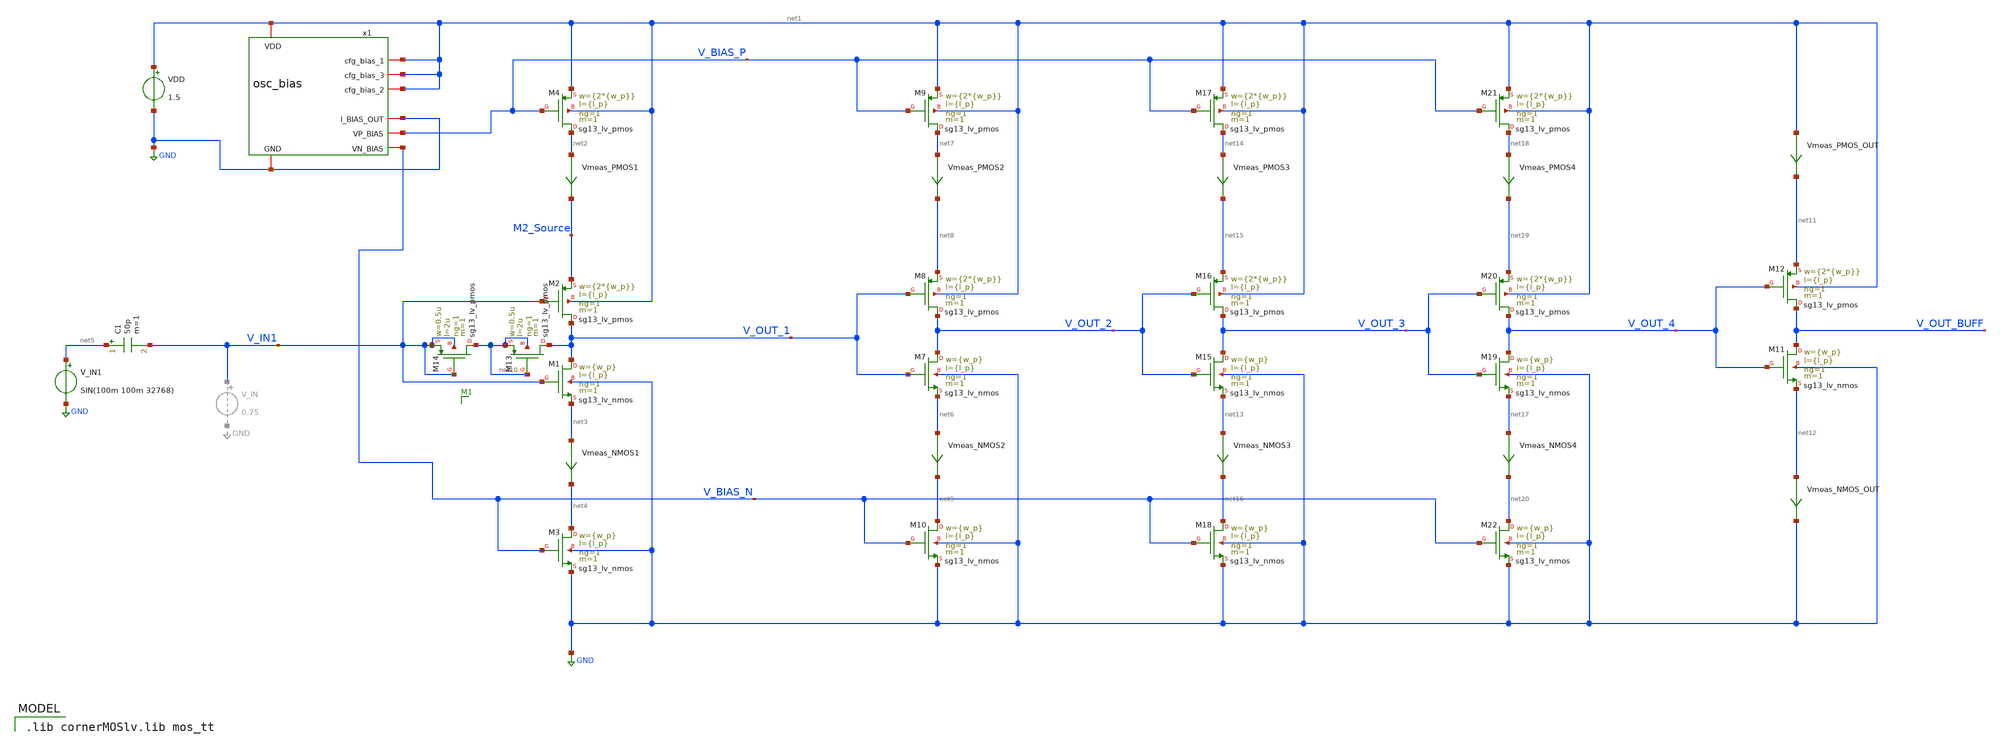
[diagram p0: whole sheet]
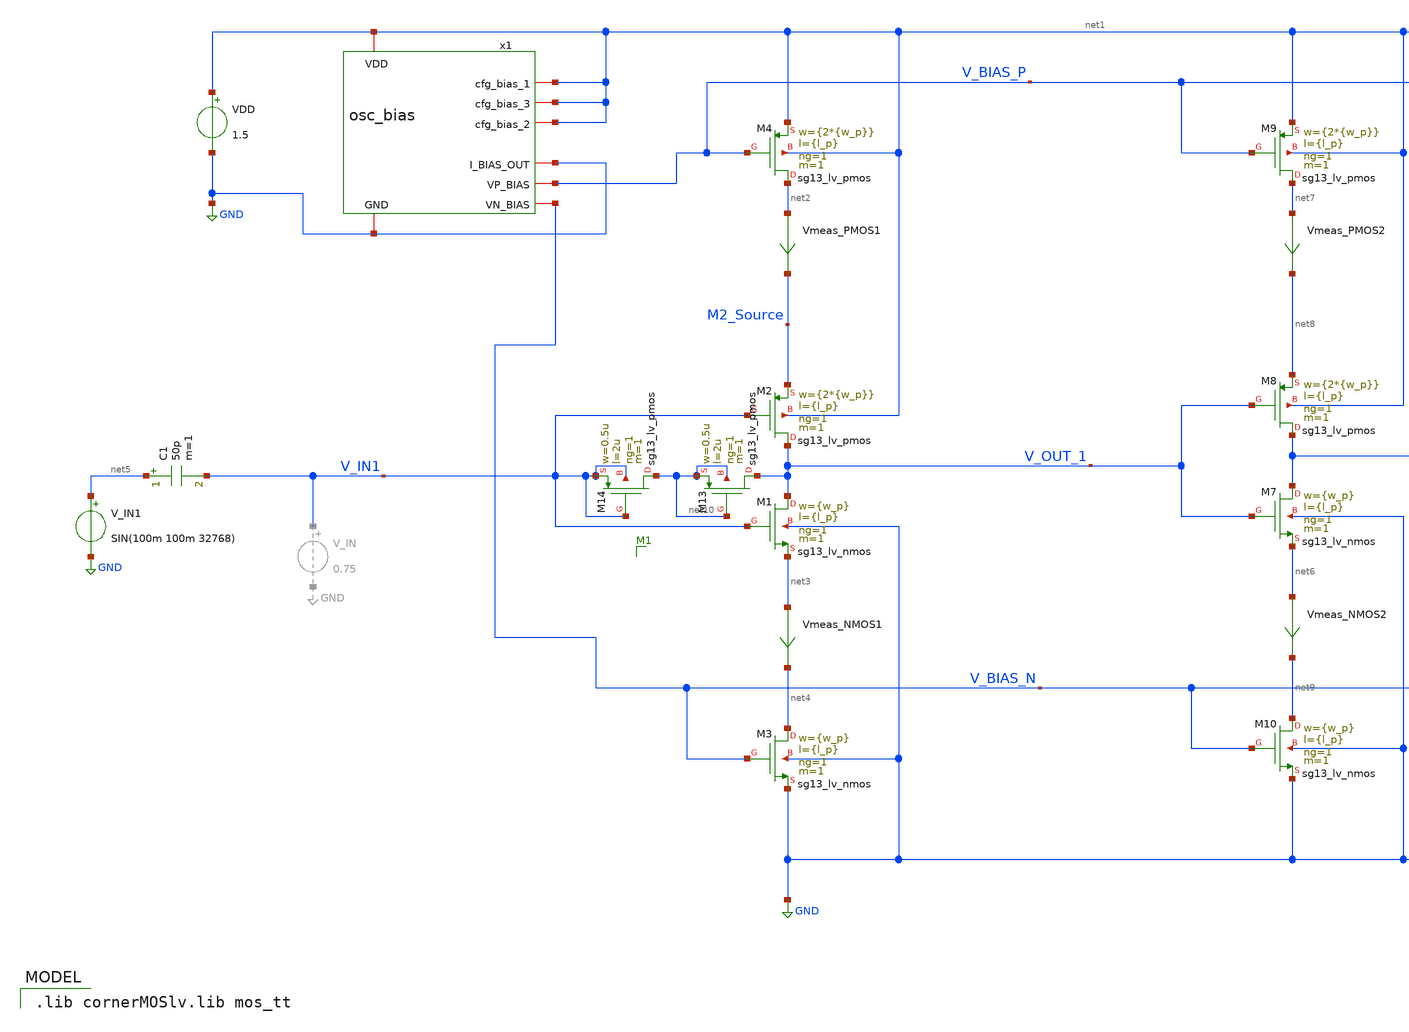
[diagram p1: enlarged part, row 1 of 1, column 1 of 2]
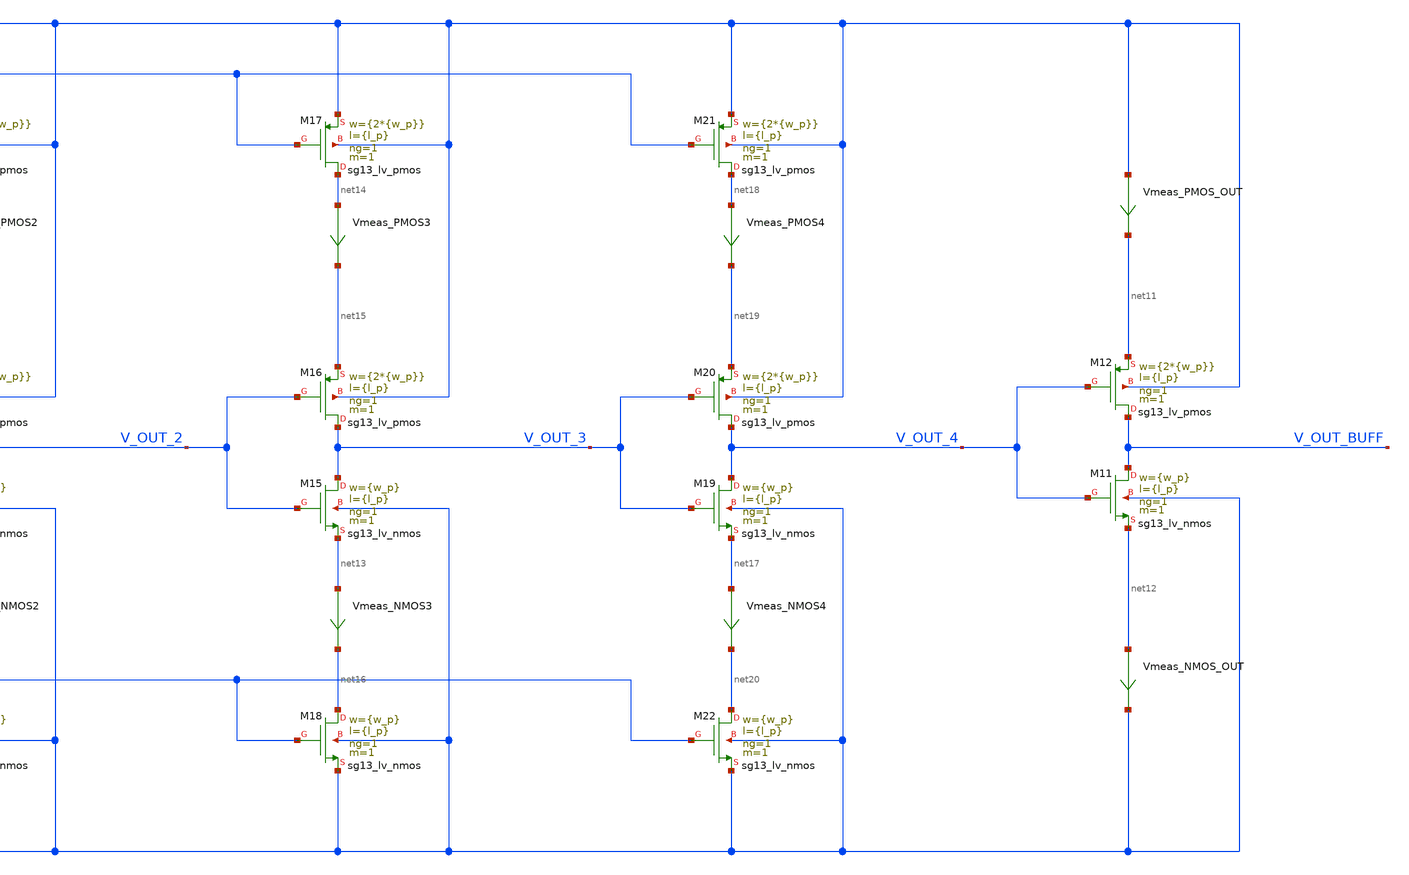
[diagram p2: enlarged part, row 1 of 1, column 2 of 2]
** sch_path: inverter_starved_v2_playground.sch
**.subckt inverter_starved_v2_playground
XM1 V_OUT_1 V_IN1 net3 GND sg13_lv_nmos w={w_p} l={l_p} ng=1 m=1 mm_ok=1
XM2 V_OUT_1 V_IN1 M2_Source net1 sg13_lv_pmos w={2*{w_p}} l={l_p} ng=1 m=1 mm_ok=1
VDD net1 GND 1.5
XM3 net4 V_BIAS_N GND GND sg13_lv_nmos w={w_p} l={l_p} ng=1 m=1 mm_ok=1
XM4 net2 V_BIAS_P net1 net1 sg13_lv_pmos w={2*{w_p}} l={l_p} ng=1 m=1 mm_ok=1
Vmeas_PMOS1 net2 M2_Source 0
.save i(vmeas_pmos1)
Vmeas_NMOS1 net3 net4 0
.save i(vmeas_nmos1)
V_IN1 net5 GND SIN(100m 100m 32768)
C1 net5 V_IN1 50p m=1
XM7 V_OUT_2 V_OUT_1 net6 GND sg13_lv_nmos w={w_p} l={l_p} ng=1 m=1 mm_ok=1
XM8 V_OUT_2 V_OUT_1 net8 net1 sg13_lv_pmos w={2*{w_p}} l={l_p} ng=1 m=1 mm_ok=1
Vmeas_NMOS2 net6 net9 0
.save i(vmeas_nmos2)
XM9 net7 V_BIAS_P net1 net1 sg13_lv_pmos w={2*{w_p}} l={l_p} ng=1 m=1 mm_ok=1
Vmeas_PMOS2 net7 net8 0
.save i(vmeas_pmos2)
XM10 net9 V_BIAS_N GND GND sg13_lv_nmos w={w_p} l={l_p} ng=1 m=1 mm_ok=1
XM11 V_OUT_BUFF V_OUT_4 net12 GND sg13_lv_nmos w={w_p} l={l_p} ng=1 m=1 mm_ok=1
XM12 V_OUT_BUFF V_OUT_4 net11 net1 sg13_lv_pmos w={2*{w_p}} l={l_p} ng=1 m=1 mm_ok=1
XM13 V_OUT_1 net10 net10 net10 sg13_lv_pmos w=0.5u l=2u ng=1 m=1 mm_ok=1
XM14 net10 V_IN1 V_IN1 V_IN1 sg13_lv_pmos w=0.5u l=2u ng=1 m=1 mm_ok=1
Vmeas_PMOS_OUT net1 net11 0
.save i(vmeas_pmos_out)
Vmeas_NMOS_OUT net12 GND 0
.save i(vmeas_nmos_out)
XM15 V_OUT_3 V_OUT_2 net13 GND sg13_lv_nmos w={w_p} l={l_p} ng=1 m=1 mm_ok=1
XM16 V_OUT_3 V_OUT_2 net15 net1 sg13_lv_pmos w={2*{w_p}} l={l_p} ng=1 m=1 mm_ok=1
Vmeas_NMOS3 net13 net16 0
.save i(vmeas_nmos3)
XM17 net14 V_BIAS_P net1 net1 sg13_lv_pmos w={2*{w_p}} l={l_p} ng=1 m=1 mm_ok=1
Vmeas_PMOS3 net14 net15 0
.save i(vmeas_pmos3)
XM18 net16 V_BIAS_N GND GND sg13_lv_nmos w={w_p} l={l_p} ng=1 m=1 mm_ok=1
XM19 V_OUT_4 V_OUT_3 net17 GND sg13_lv_nmos w={w_p} l={l_p} ng=1 m=1 mm_ok=1
XM20 V_OUT_4 V_OUT_3 net19 net1 sg13_lv_pmos w={2*{w_p}} l={l_p} ng=1 m=1 mm_ok=1
Vmeas_NMOS4 net17 net20 0
.save i(vmeas_nmos4)
XM21 net18 V_BIAS_P net1 net1 sg13_lv_pmos w={2*{w_p}} l={l_p} ng=1 m=1 mm_ok=1
Vmeas_PMOS4 net18 net19 0
.save i(vmeas_pmos4)
XM22 net20 V_BIAS_N GND GND sg13_lv_nmos w={w_p} l={l_p} ng=1 m=1 mm_ok=1
x1 net1 net1 net1 net1 GND GND V_BIAS_P V_BIAS_N osc_bias
**** begin user architecture code
 .lib cornerMOSlv.lib mos_tt



.include inverter_starved_v2_playground.save
.param w_p=0.40u l_p=0.13u
.meas tran iavg_stage_1_pmos AVG i(Vmeas_PMOS1)
.meas tran iavg_stage_1_nmos AVG i(Vmeas_NMOS2)
.meas tran iavg_stage_2_pmos AVG i(Vmeas_PMOS2)
.meas tran iavg_stage_2_nmos AVG i(Vmeas_NMOS2)
.meas tran iavg_stage_3_pmos AVG i(Vmeas_PMOS3)
.meas tran iavg_stage_3_nmos AVG i(Vmeas_NMOS3)
.meas tran iavg_stage_4_pmos AVG i(Vmeas_PMOS4)
.meas tran iavg_stage_4_nmos AVG i(Vmeas_NMOS4)
.meas tran iavg_stage_5_pmos AVG i(Vmeas_PMOS_OUT)
.meas tran iavg_stage_5_nmos AVG i(Vmeas_NMOS_OUT)
.meas tran iavg_VDD AVG i(VDD)

.control
save all


tran 0.0001m 0.2m

*plot V_IN1 V_OUT_1 V_OUT_2 V_OUT_3 V_OUT_4 V_OUT_BUFF
plot V_IN1 V_OUT_BUFF


*fft V_OUT_3
*plot mag(V_OUT_3)

*.measure tran yrms RMS i(VDD) from=0.1m to=0.2m

.endc


**** end user architecture code
**.ends

* expanding   symbol:  osc_bias.sym # of pins=8
** sym_path: osc_bias.sym
** sch_path: osc_bias.sch
.subckt osc_bias VDD cfg_bias_1 cfg_bias_3 cfg_bias_2 GND I_BIAS_OUT VP_BIAS VN_BIAS
*.iopin VDD
*.iopin GND
*.iopin I_BIAS_OUT
*.iopin cfg_bias_1
*.iopin cfg_bias_2
*.iopin cfg_bias_3
*.opin VN_BIAS
*.opin VP_BIAS
XM1 VP_BIAS VP_BIAS VDD VDD sg13_lv_pmos w=0.2u l=0.13u ng=1 m=1 mm_ok=1
XM3 VP_BIAS VP_BIAS net1 GND sg13_lv_nmos w=0.2u l=10u ng=1 m=1 mm_ok=1
XM4 net1 net1 net2 GND sg13_lv_nmos w=0.2u l=10u ng=1 m=1 mm_ok=1
XM5 net2 net2 VN_BIAS GND sg13_lv_nmos w=0.2u l=10u ng=1 m=1 mm_ok=1
XM2 net6 VP_BIAS VDD VDD sg13_lv_pmos w=0.25u l=10u ng=1 m=2 mm_ok=1
XM6 I_BIAS_OUT cfg_bias_1 net6 VDD sg13_lv_pmos w=0.25u l=10u ng=1 m=1 mm_ok=1
XM7 net3 VP_BIAS VDD VDD sg13_lv_pmos w=0.25u l=10u ng=1 m=4 mm_ok=1
XM8 net4 VP_BIAS VDD VDD sg13_lv_pmos w=0.25u l=10u ng=1 m=20 mm_ok=1
XM9 I_BIAS_OUT cfg_bias_2 net3 VDD sg13_lv_pmos w=0.5u l=10u ng=1 m=1 mm_ok=1
XM10 I_BIAS_OUT cfg_bias_3 net4 VDD sg13_lv_pmos w=1u l=10u ng=1 m=1 mm_ok=1
XM11 VN_BIAS VN_BIAS net5 GND sg13_lv_nmos w=0.2u l=0.13u ng=1 m=1 mm_ok=1
Vmeas net5 GND 0
.save i(vmeas)
.ends

.GLOBAL GND
.end
